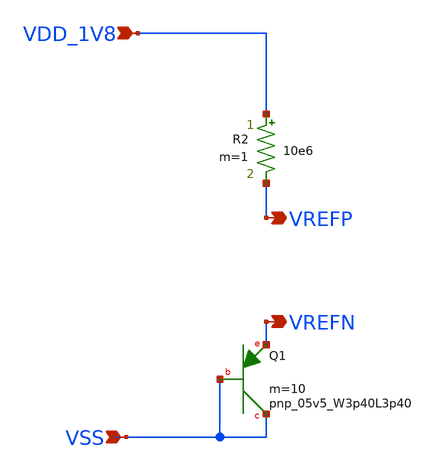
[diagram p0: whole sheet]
** sch_path: design/CNR_GR02_SKY130NM/CNR_GR02.sch
**.subckt CNR_GR02 VDD_1V8 VSS VREFP VREFN
*.ipin VDD_1V8
*.ipin VSS
*.opin VREFP
*.opin VREFN
R2 VDD_1V8 VREFP 10e6 m=1
XQ1 VSS VSS VREFN sky130_fd_pr__pnp_05v5_W3p40L3p40 m=10
**.ends
.end
